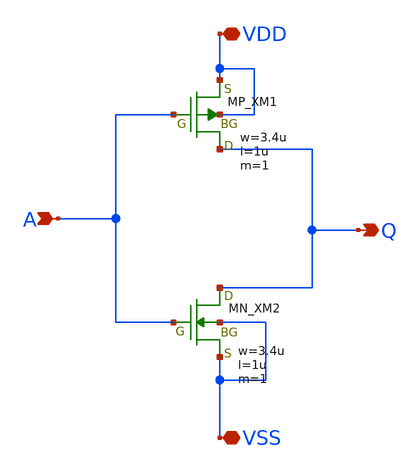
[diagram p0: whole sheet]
** sch_path: schematic/20250924_OSS_Workshop/Qdai/inverter_MUX_01/inv_CHEN_02.sch
**.subckt inv_CHEN_02 VDD Q VSS A
*.iopin VDD
*.opin Q
*.iopin VSS
*.ipin A
XM1 Q A VDD VDD PMOS w=3.4u l=1u as=0 ad=0 ps=0 pd=0 nrd=0 nrs=0 m=1
XM2 Q A VSS VSS NMOS w=3.4u l=1u as=0 ad=0 ps=0 pd=0 nrd=0 nrs=0 m=1
**.ends
.end
